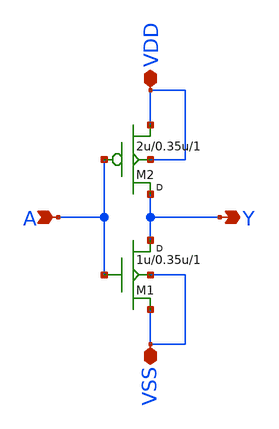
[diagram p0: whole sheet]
** sch_path: examples/buffer/libs/logic/inv/schematic/inv.sch
**.subckt inv A Y VDD VSS
*.ipin A
*.opin Y
*.iopin VDD
*.iopin VSS
M2 Y A VDD VDD pmos w=2u l=0.35u m=1
M1 Y A VSS VSS nmos w=1u l=0.35u m=1
**.ends
.end
